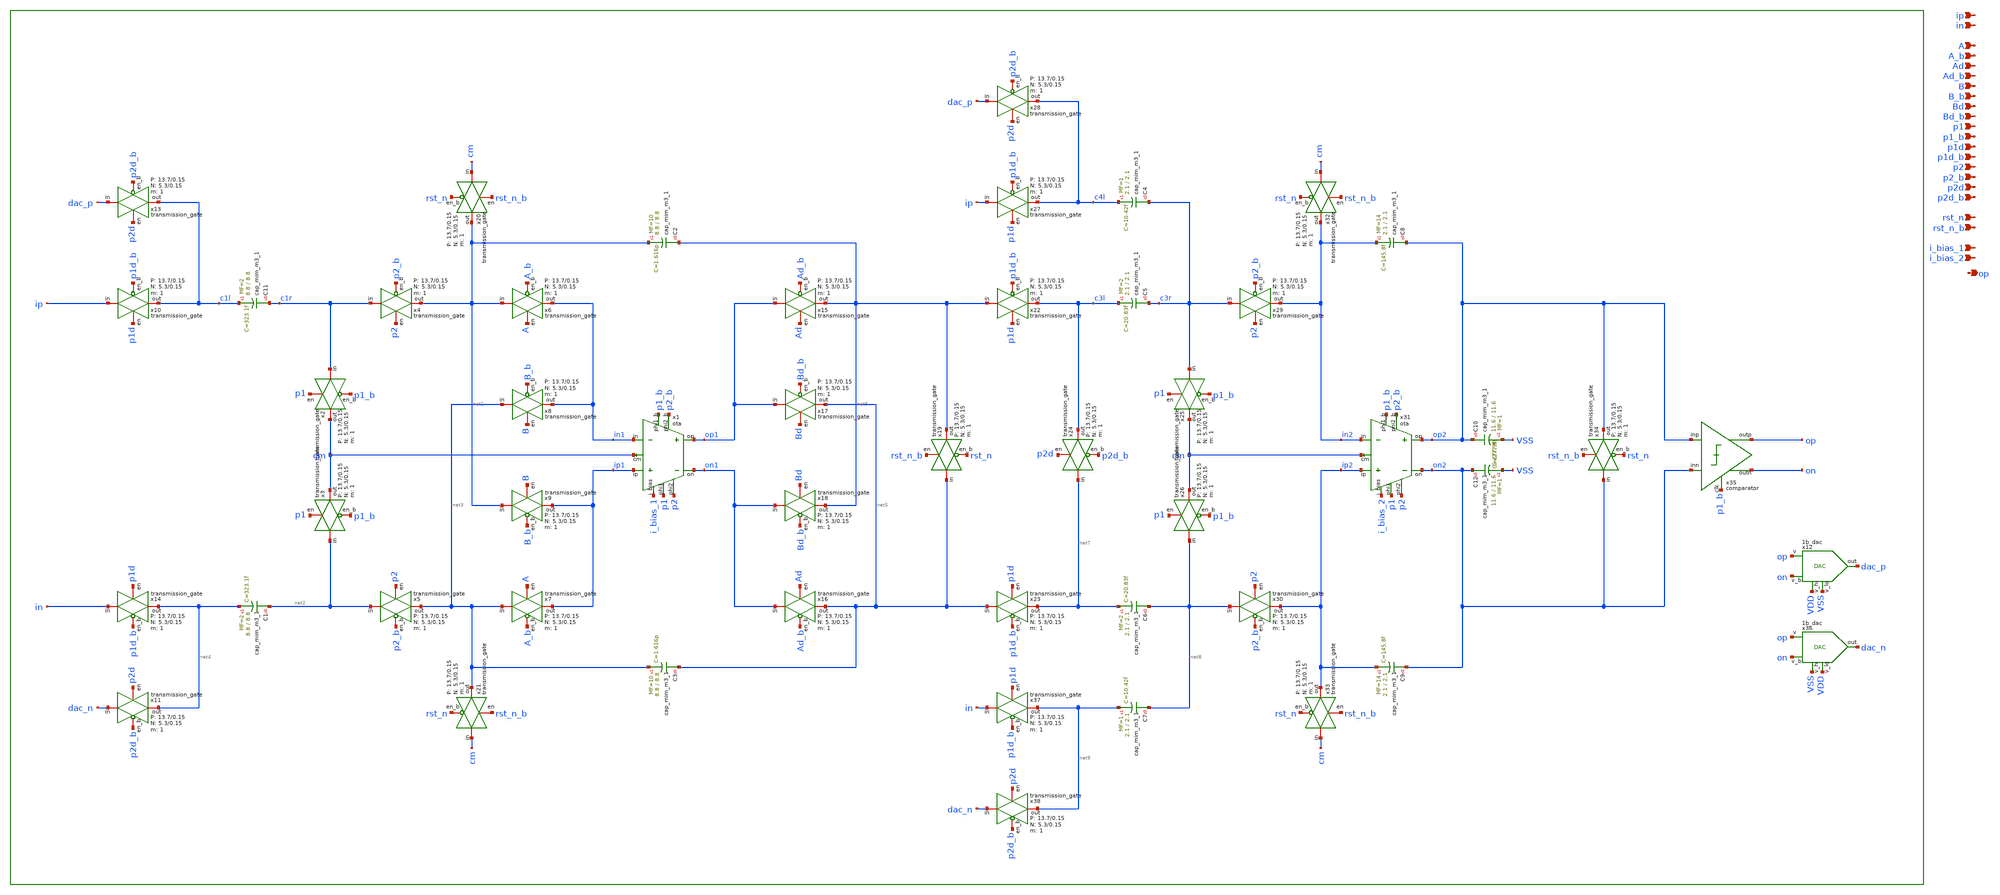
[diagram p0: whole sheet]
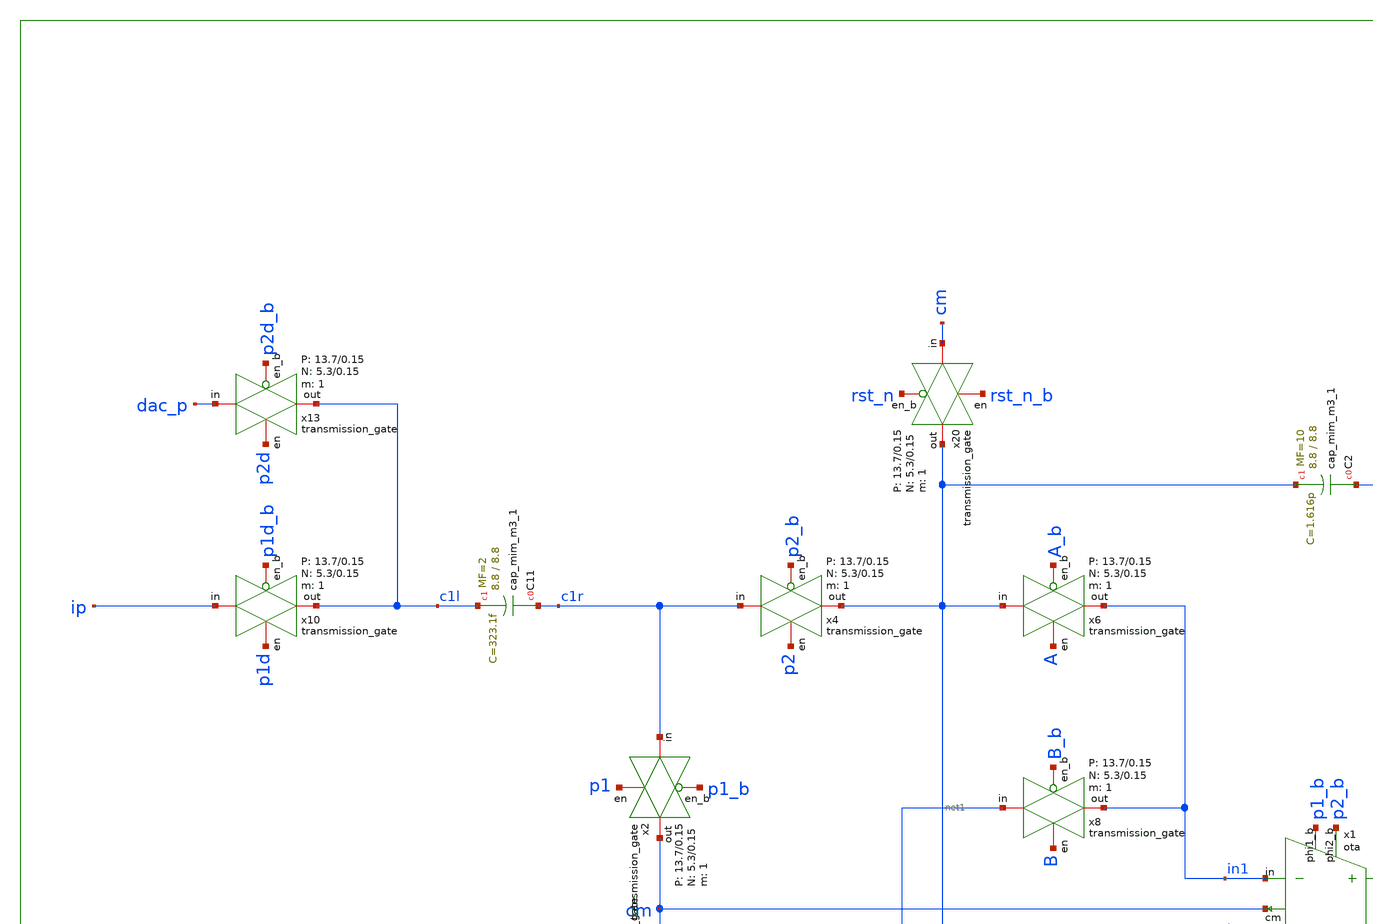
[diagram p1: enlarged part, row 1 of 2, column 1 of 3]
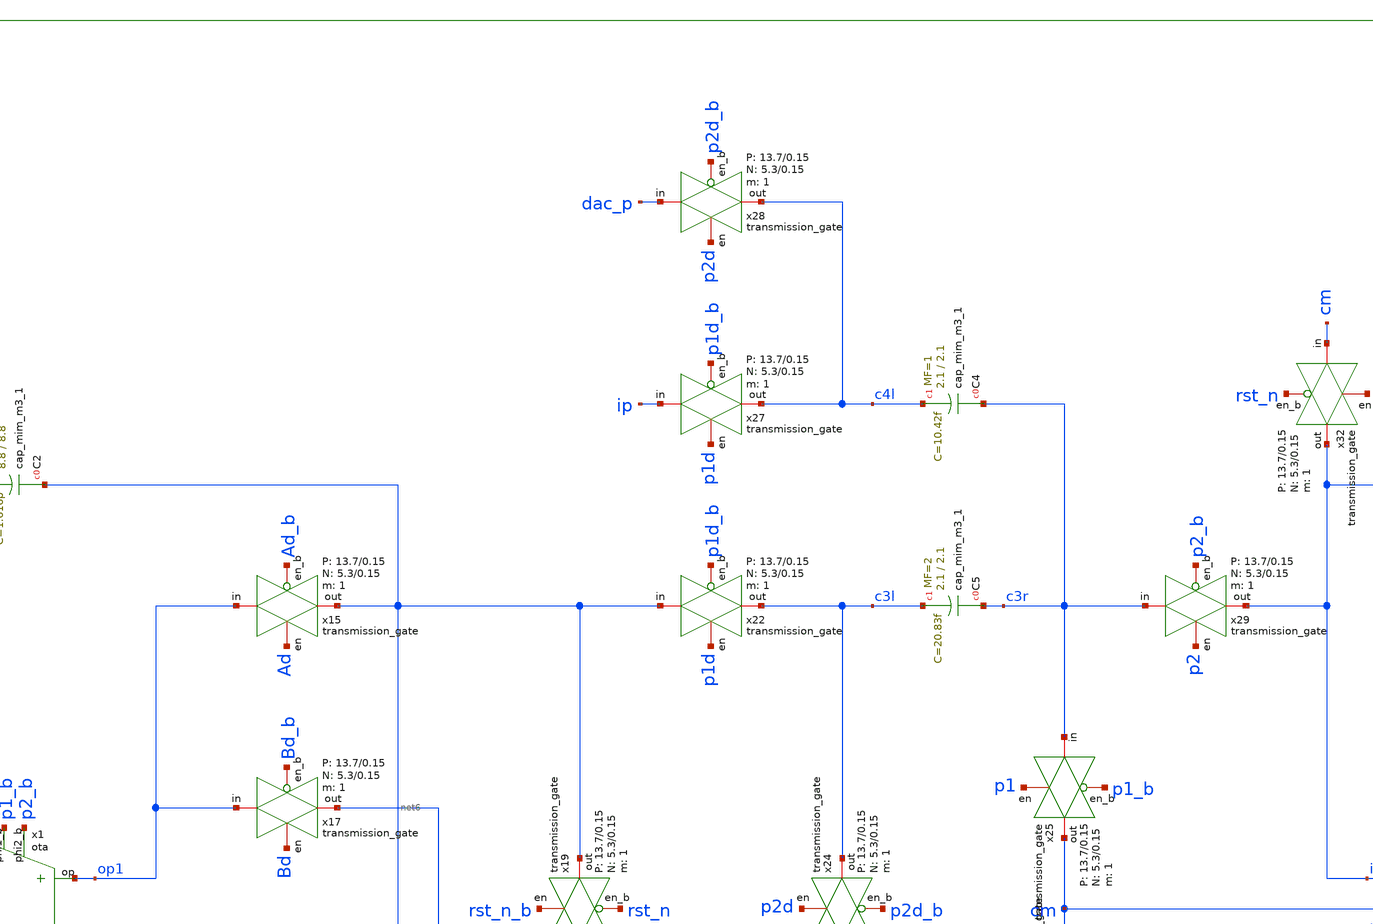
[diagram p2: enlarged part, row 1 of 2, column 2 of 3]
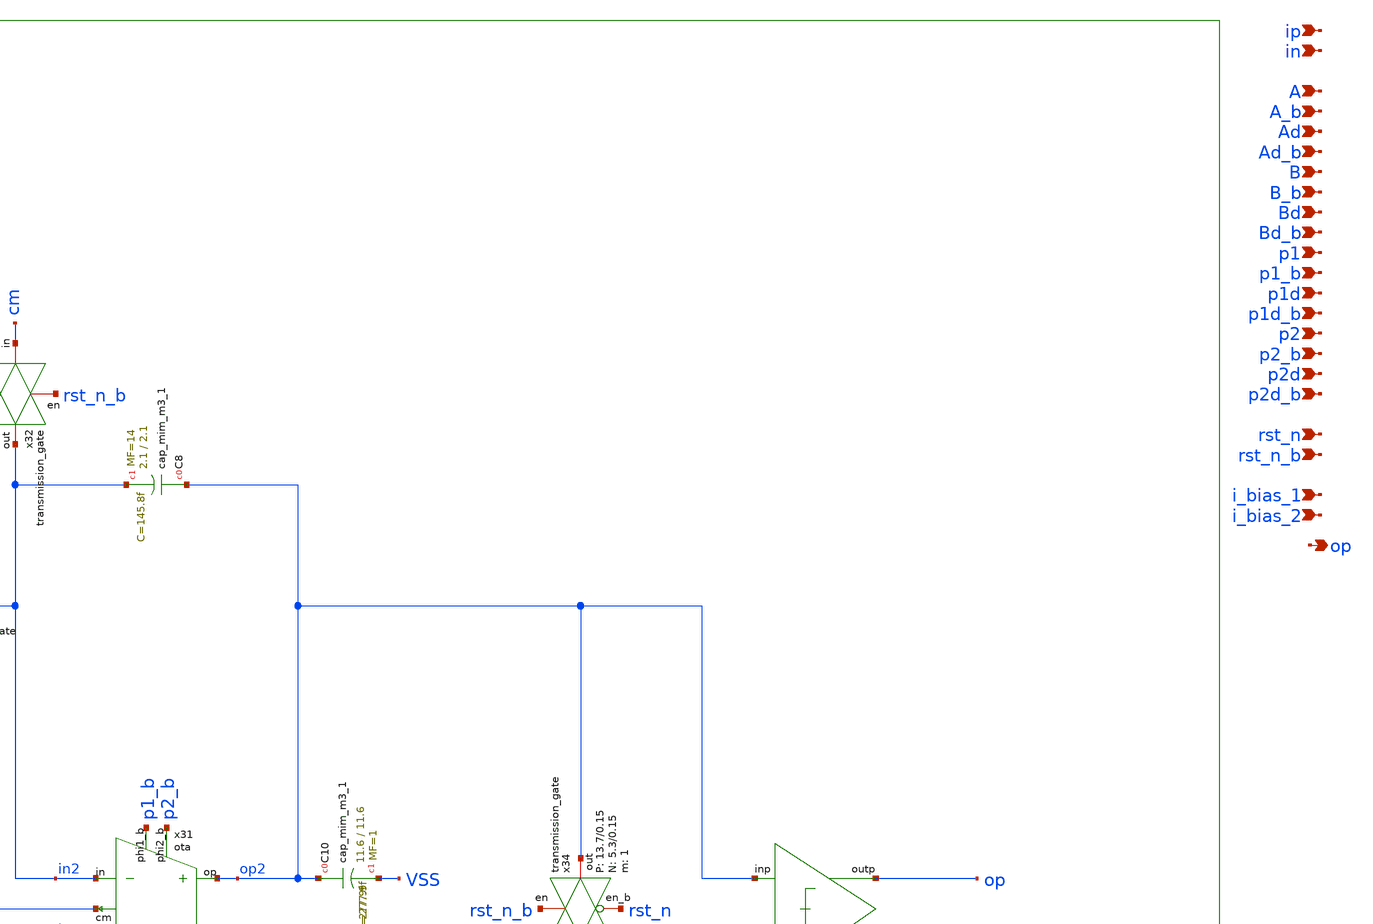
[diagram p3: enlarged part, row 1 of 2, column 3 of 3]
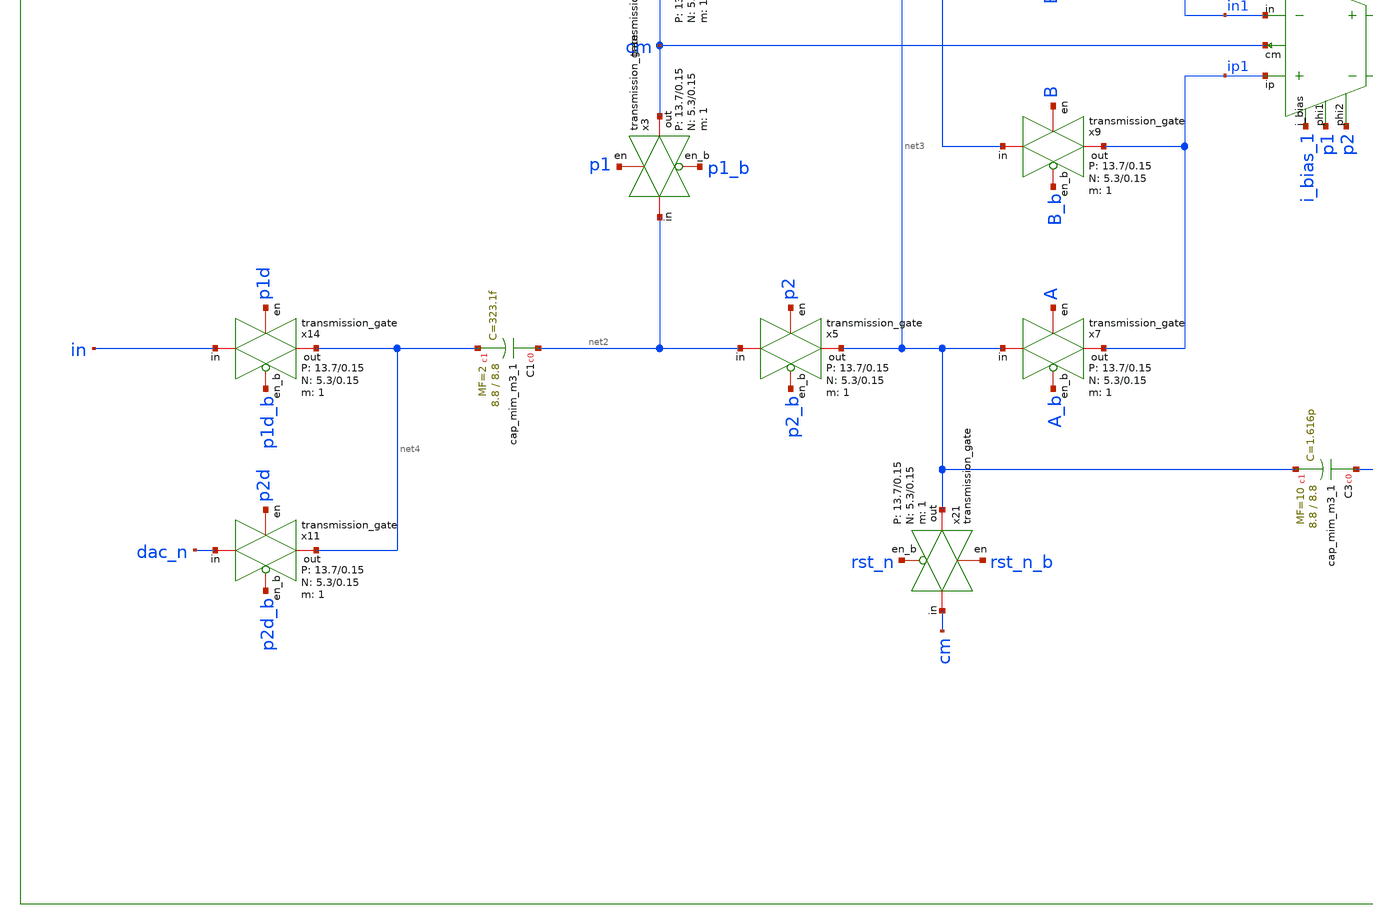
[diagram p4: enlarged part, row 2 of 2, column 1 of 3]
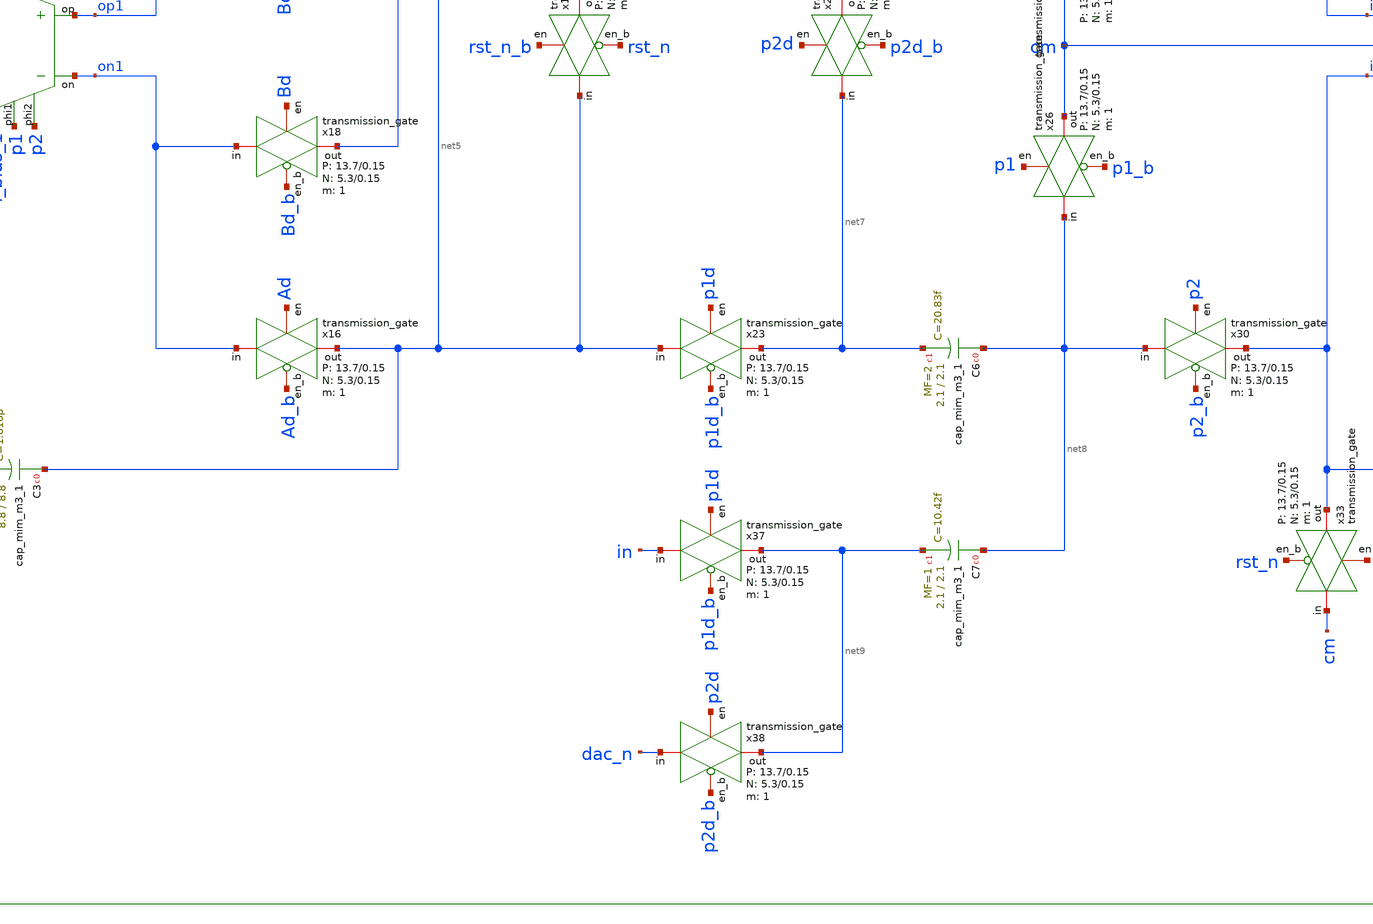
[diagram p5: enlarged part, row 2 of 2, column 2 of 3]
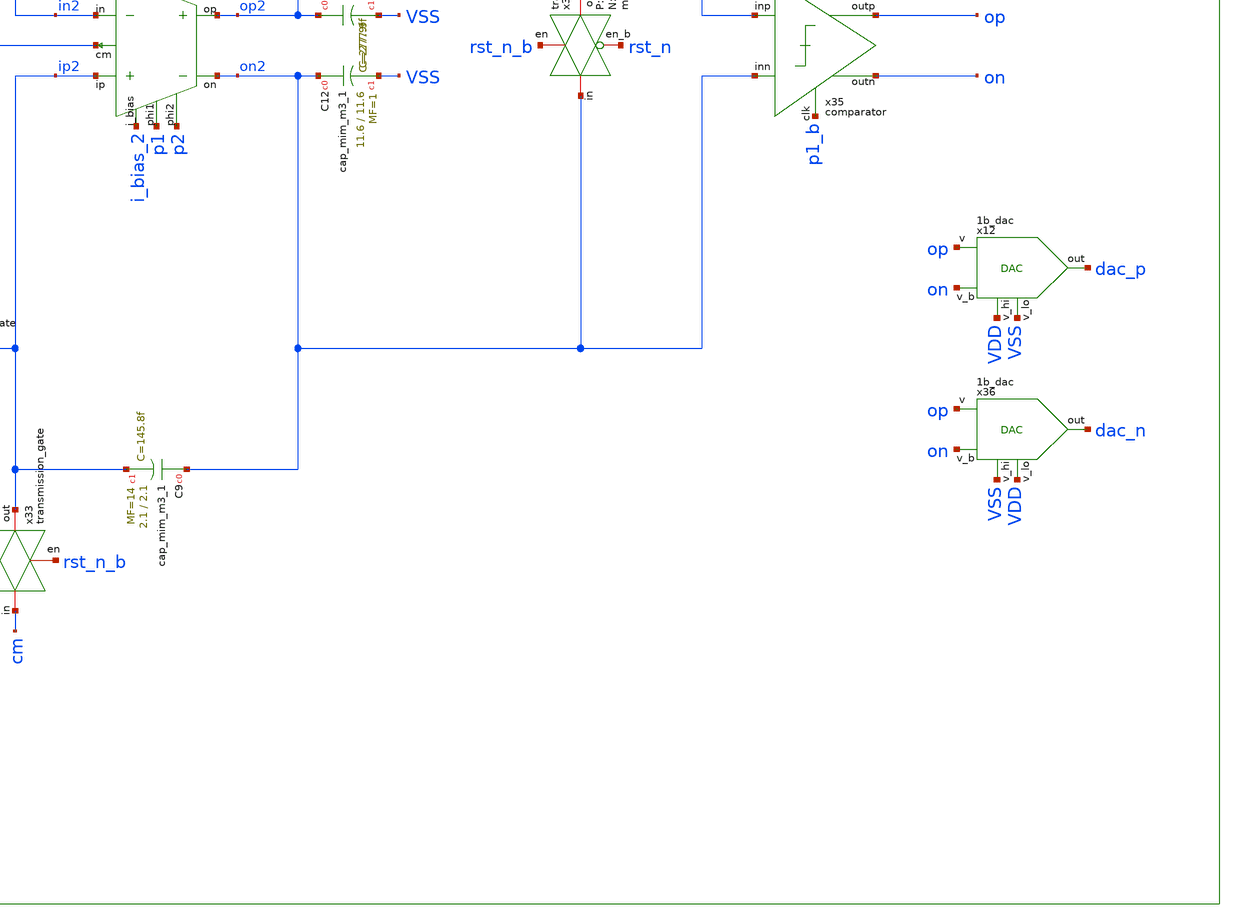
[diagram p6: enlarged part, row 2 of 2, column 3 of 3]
** sch_path: design/analog_modulator/schematic/modulator.sch
**.subckt modulator ip in A A_b Ad Ad_b B B_b Bd Bd_b p1 p1_b p1d p1d_b p2 p2_b p2d p2d_b rst_n
*+ rst_n_b i_bias_1 i_bias_2 op
*.ipin ip
*.ipin in
*.ipin A
*.ipin A_b
*.ipin Ad
*.ipin Ad_b
*.ipin B
*.ipin B_b
*.ipin Bd
*.ipin Bd_b
*.ipin p1
*.ipin p1_b
*.ipin p1d
*.ipin p1d_b
*.ipin p2
*.ipin p2_b
*.ipin p2d
*.ipin p2d_b
*.ipin rst_n
*.ipin rst_n_b
*.ipin i_bias_1
*.ipin i_bias_2
*.opin op
x4 c1r net1 p2 p2_b VDD VSS 1 5.3 0.15 13.7 0.15 transmission_gate
x5 net2 net3 p2 p2_b VDD VSS 1 5.3 0.15 13.7 0.15 transmission_gate
x2 c1r cm p1 p1_b VDD VSS 1 5.3 0.15 13.7 0.15 transmission_gate
x3 net2 cm p1 p1_b VDD VSS 1 5.3 0.15 13.7 0.15 transmission_gate
x10 ip c1l p1d p1d_b VDD VSS 1 5.3 0.15 13.7 0.15 transmission_gate
x11 dac_n net4 p2d p2d_b VDD VSS 1 5.3 0.15 13.7 0.15 transmission_gate
x12 VDD VSS op dac_p on VDD VSS 1b_dac
x13 dac_p c1l p2d p2d_b VDD VSS 1 5.3 0.15 13.7 0.15 transmission_gate
x14 in net4 p1d p1d_b VDD VSS 1 5.3 0.15 13.7 0.15 transmission_gate
x19 net5 net6 rst_n_b rst_n VDD VSS 1 5.3 0.15 13.7 0.15 transmission_gate
x20 cm net1 rst_n_b rst_n VDD VSS 1 5.3 0.15 13.7 0.15 transmission_gate
x21 cm net3 rst_n_b rst_n VDD VSS 1 5.3 0.15 13.7 0.15 transmission_gate
x22 net6 c3l p1d p1d_b VDD VSS 1 5.3 0.15 13.7 0.15 transmission_gate
x23 net5 net7 p1d p1d_b VDD VSS 1 5.3 0.15 13.7 0.15 transmission_gate
x24 net7 c3l p2d p2d_b VDD VSS 1 5.3 0.15 13.7 0.15 transmission_gate
x25 c3r cm p1 p1_b VDD VSS 1 5.3 0.15 13.7 0.15 transmission_gate
x26 net8 cm p1 p1_b VDD VSS 1 5.3 0.15 13.7 0.15 transmission_gate
x27 ip c4l p1d p1d_b VDD VSS 1 5.3 0.15 13.7 0.15 transmission_gate
x28 dac_p c4l p2d p2d_b VDD VSS 1 5.3 0.15 13.7 0.15 transmission_gate
x29 c3r in2 p2 p2_b VDD VSS 1 5.3 0.15 13.7 0.15 transmission_gate
x30 net8 ip2 p2 p2_b VDD VSS 1 5.3 0.15 13.7 0.15 transmission_gate
x32 cm in2 rst_n_b rst_n VDD VSS 1 5.3 0.15 13.7 0.15 transmission_gate
x33 cm ip2 rst_n_b rst_n VDD VSS 1 5.3 0.15 13.7 0.15 transmission_gate
x34 on2 op2 rst_n_b rst_n VDD VSS 1 5.3 0.15 13.7 0.15 transmission_gate
x36 VSS VDD op dac_n on VDD VSS 1b_dac
x37 in net9 p1d p1d_b VDD VSS 1 5.3 0.15 13.7 0.15 transmission_gate
x38 dac_n net9 p2d p2d_b VDD VSS 1 5.3 0.15 13.7 0.15 transmission_gate
XC11 c1r c1l sky130_fd_pr__cap_mim_m3_1 W=8.8 L=8.8 MF=2 m=2
XC1 net2 net4 sky130_fd_pr__cap_mim_m3_1 W=8.8 L=8.8 MF=2 m=2
XC2 net6 net1 sky130_fd_pr__cap_mim_m3_1 W=8.8 L=8.8 MF=10 m=10
XC3 net5 net3 sky130_fd_pr__cap_mim_m3_1 W=8.8 L=8.8 MF=10 m=10
XC4 c3r c4l sky130_fd_pr__cap_mim_m3_1 W=2.1 L=2.1 MF=1 m=1
XC5 c3r c3l sky130_fd_pr__cap_mim_m3_1 W=2.1 L=2.1 MF=2 m=2
XC6 net8 net7 sky130_fd_pr__cap_mim_m3_1 W=2.1 L=2.1 MF=2 m=2
XC7 net8 net9 sky130_fd_pr__cap_mim_m3_1 W=2.1 L=2.1 MF=1 m=1
XC8 op2 in2 sky130_fd_pr__cap_mim_m3_1 W=2.1 L=2.1 MF=14 m=14
XC9 on2 ip2 sky130_fd_pr__cap_mim_m3_1 W=2.1 L=2.1 MF=14 m=14
XC10 op2 VSS sky130_fd_pr__cap_mim_m3_1 W=11.6 L=11.6 MF=1 m=1
XC12 on2 VSS sky130_fd_pr__cap_mim_m3_1 W=11.6 L=11.6 MF=1 m=1
x6 net1 in1 A A_b VDD VSS 1 5.3 0.15 13.7 0.15 transmission_gate
x8 net3 in1 B B_b VDD VSS 1 5.3 0.15 13.7 0.15 transmission_gate
x15 op1 net6 Ad Ad_b VDD VSS 1 5.3 0.15 13.7 0.15 transmission_gate
x16 on1 net5 Ad Ad_b VDD VSS 1 5.3 0.15 13.7 0.15 transmission_gate
x17 op1 net5 Bd Bd_b VDD VSS 1 5.3 0.15 13.7 0.15 transmission_gate
x18 on1 net6 Bd Bd_b VDD VSS 1 5.3 0.15 13.7 0.15 transmission_gate
x1 i_bias_1 ip1 in1 p1 p1_b p2 p2_b op1 on1 cm VDD VSS ota
x31 i_bias_2 ip2 in2 p1 p1_b p2 p2_b op2 on2 cm VDD VSS ota
x35 op2 on2 op p1_b on VDD VSS comparator
x7 net3 ip1 A A_b VDD VSS 1 5.3 0.15 13.7 0.15 transmission_gate
x9 net1 ip1 B B_b VDD VSS 1 5.3 0.15 13.7 0.15 transmission_gate
**.ends
.end
